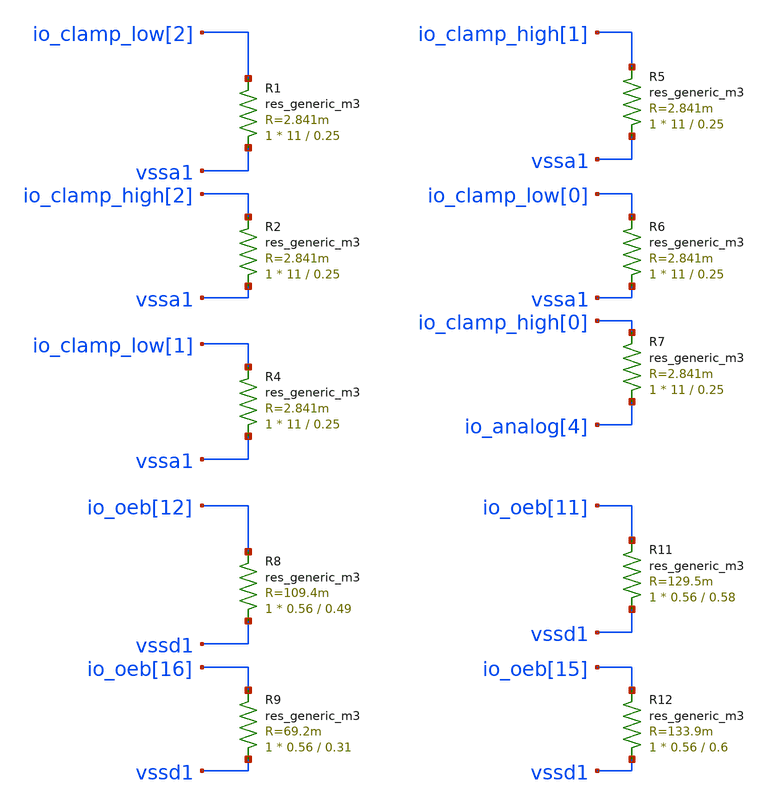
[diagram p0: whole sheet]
** sch_path: xschem/por_tie.sch
**.subckt por_tie
R1 vssa1 io_clamp_low[2] sky130_fd_pr__res_generic_m3 W=11 L=0.25 m=1
R2 vssa1 io_clamp_high[2] sky130_fd_pr__res_generic_m3 W=11 L=0.25 m=1
R4 vssa1 io_clamp_low[1] sky130_fd_pr__res_generic_m3 W=11 L=0.25 m=1
R5 vssa1 io_clamp_high[1] sky130_fd_pr__res_generic_m3 W=11 L=0.25 m=1
R6 vssa1 io_clamp_low[0] sky130_fd_pr__res_generic_m3 W=11 L=0.25 m=1
R7 io_analog[4] io_clamp_high[0] sky130_fd_pr__res_generic_m3 W=11 L=0.25 m=1
R8 vssd1 io_oeb[12] sky130_fd_pr__res_generic_m3 W=0.56 L=0.49 m=1
R9 vssd1 io_oeb[16] sky130_fd_pr__res_generic_m3 W=0.56 L=0.31 m=1
R11 vssd1 io_oeb[11] sky130_fd_pr__res_generic_m3 W=0.56 L=0.58 m=1
R12 vssd1 io_oeb[15] sky130_fd_pr__res_generic_m3 W=0.56 L=0.6 m=1
**.ends
.end
